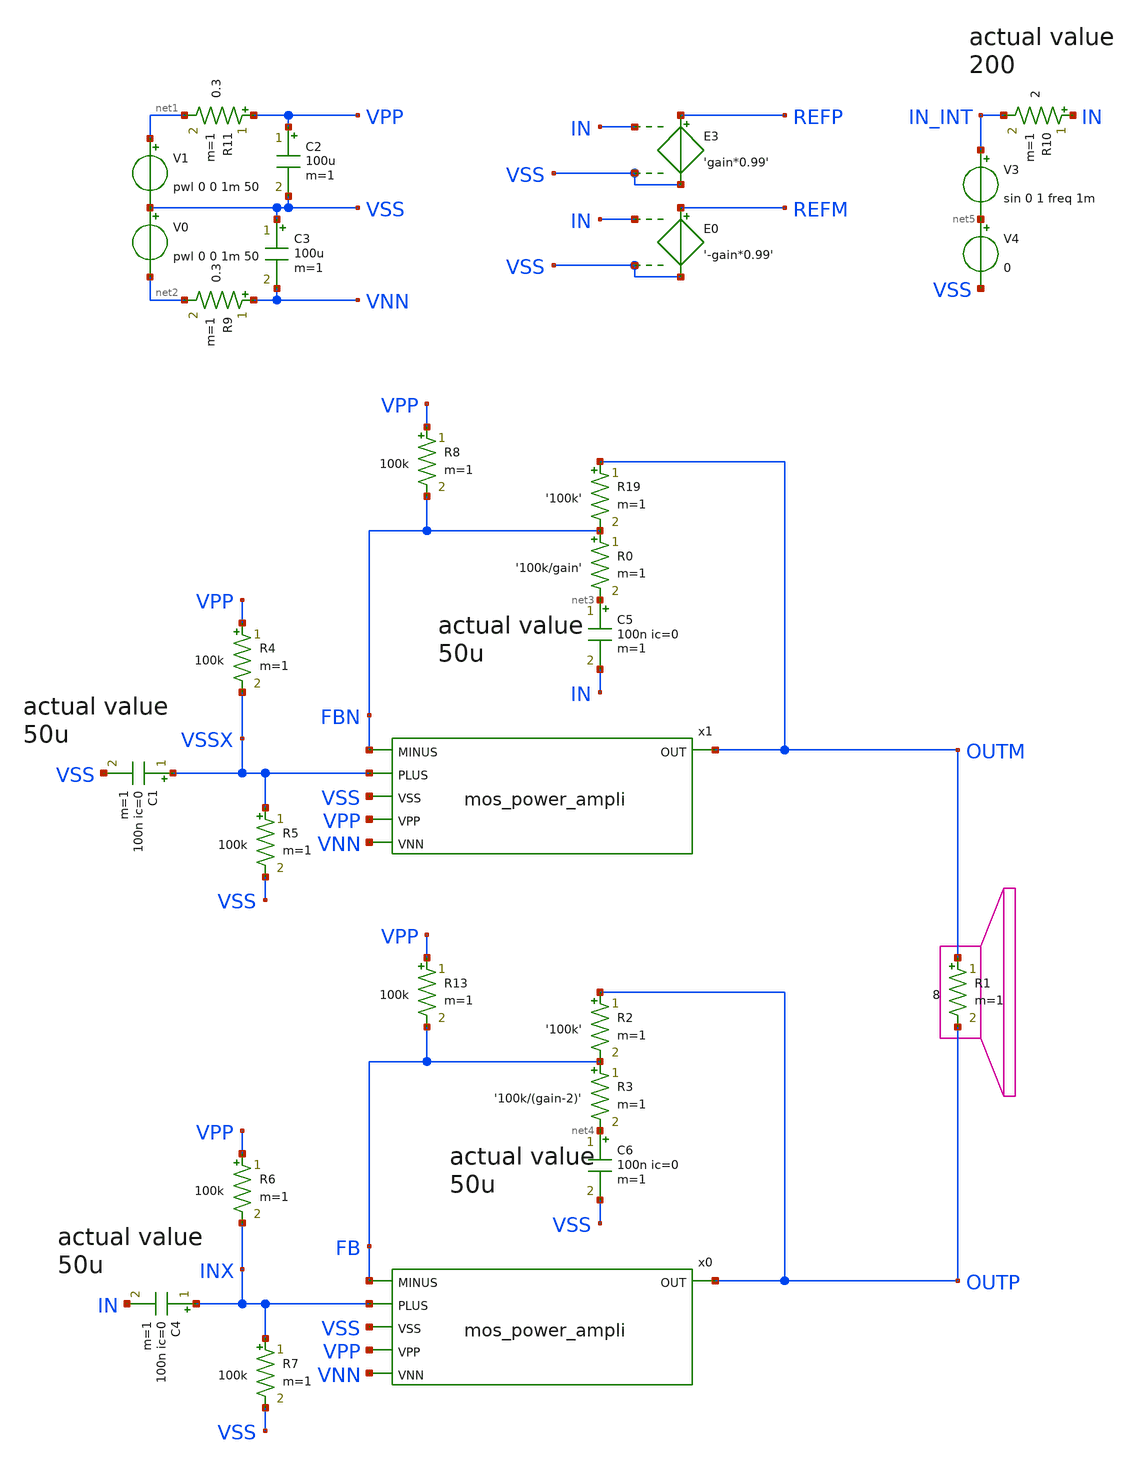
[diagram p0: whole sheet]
** sch_path: xschem_library/examples/poweramp.sch
**.subckt poweramp
V1 net1 VSS pwl 0 0 1m 50
V0 VSS net2 pwl 0 0 1m 50
R1 OUTM OUTP 8 m=1
E3 REFP VSS IN VSS 'gain*0.99'
C2 VPP VSS 100u m=1
C3 VSS VNN 100u m=1
R11 VPP net1 0.3 m=1
R9 VNN net2 0.3 m=1
R19 OUTM FBN '100k' m=1
R0 FBN net3 '100k/gain' m=1
x1 OUTM VSSX FBN VPP VNN VSS mos_power_ampli
x0 OUTP INX FB VPP VNN VSS mos_power_ampli
R6 VPP INX 100k m=1
R7 INX VSS 100k m=1
E0 REFM VSS IN VSS '-gain*0.99'
C5 net3 IN 100n ic=0 m=1
C6 net4 VSS 100n ic=0 m=1
R2 OUTP FB '100k' m=1
R3 FB net4 '100k/(gain-2)' m=1
V3 IN_INT net5 sin 0 1 freq 1m
R4 VPP VSSX 100k m=1
R5 VSSX VSS 100k m=1
R8 VPP FBN 100k m=1
C4 INX IN 100n ic=0 m=1
C1 VSSX VSS 100n ic=0 m=1
R10 IN IN_INT 2 m=1
R13 VPP FB 100k m=1
V4 net5 VSS 0
**** begin user architecture code

.option PARHIER=LOCAL RUNLVL=6 post MODMONTE=1 warn maxwarns=400
.option ITL4=20000 ITL5=0
* .option sampling_method = SRS
* .option method=gear
vvss vss 0 dc 0
.temp 30

.param freq=20k
.param gain=42
.tran '2m/freq' '1m + 160/freq' uic

** models are generally not free: you must download
** SPICE models for active devices and put them  into the below
** referenced file in netlist/simulation directory.
.include "models_poweramp.txt"
.save all
* .FOUR 20k v(outm,outp)
* .probe i(*)
* .probe p(r*) p(v*)


**** end user architecture code
**.ends
.end
